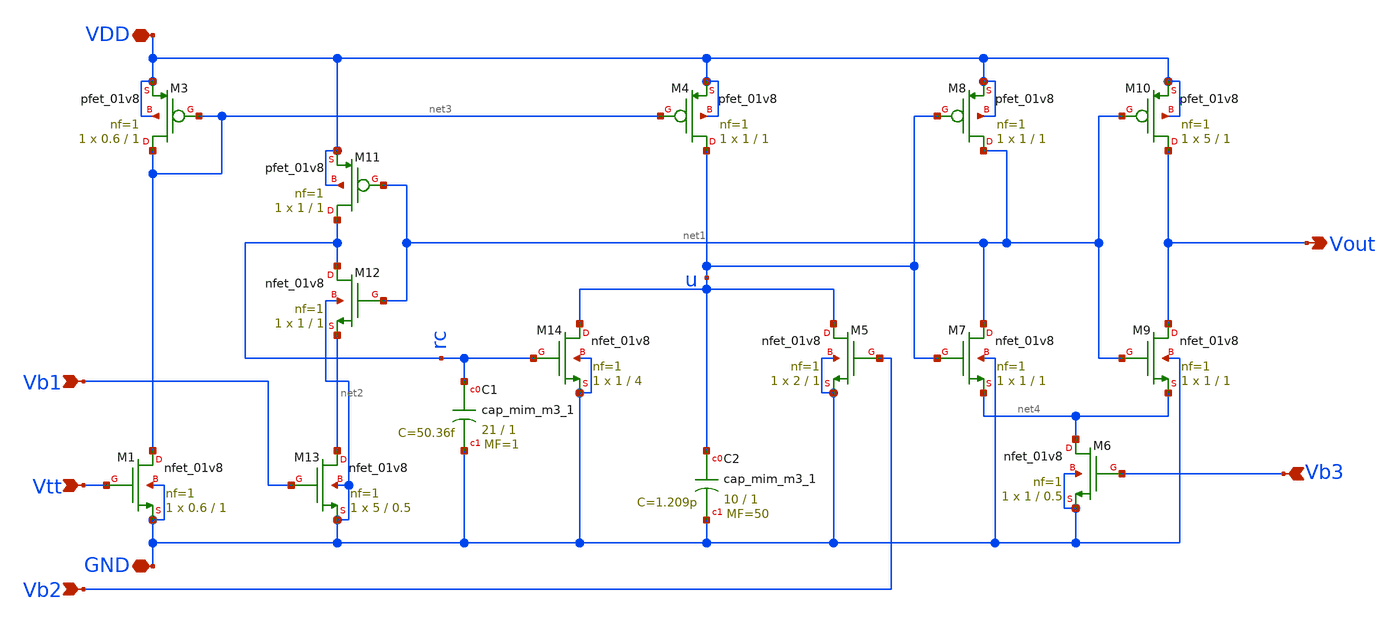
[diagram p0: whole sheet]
** sch_path: LIF_neuron/LIF_neuron_Vohra_modified.sch
**.subckt LIF_neuron_Vohra_modified Vtt GND Vb1 Vb2 VDD Vout Vb3
*.ipin Vtt
*.iopin GND
*.ipin Vb1
*.ipin Vb2
*.iopin VDD
*.opin Vout
*.ipin Vb3
XM1 net3 Vtt GND GND sky130_fd_pr__nfet_01v8 L=1 W=0.6 nf=1 ad='int((nf+1)/2) * W/nf * 0.29' as='int((nf+2)/2) * W/nf * 0.29'
+ pd='2*int((nf+1)/2) * (W/nf + 0.29)' ps='2*int((nf+2)/2) * (W/nf + 0.29)' nrd='0.29 / W' nrs='0.29 / W'
+ sa=0 sb=0 sd=0 mult=1 m=1
XM3 net3 net3 VDD VDD sky130_fd_pr__pfet_01v8 L=1 W=0.6 nf=1 ad='int((nf+1)/2) * W/nf * 0.29' as='int((nf+2)/2) * W/nf * 0.29'
+ pd='2*int((nf+1)/2) * (W/nf + 0.29)' ps='2*int((nf+2)/2) * (W/nf + 0.29)' nrd='0.29 / W' nrs='0.29 / W'
+ sa=0 sb=0 sd=0 mult=1 m=1
XM13 net2 Vb1 GND GND sky130_fd_pr__nfet_01v8 L=0.5 W=5 nf=1 ad='int((nf+1)/2) * W/nf * 0.29' as='int((nf+2)/2) * W/nf * 0.29'
+ pd='2*int((nf+1)/2) * (W/nf + 0.29)' ps='2*int((nf+2)/2) * (W/nf + 0.29)' nrd='0.29 / W' nrs='0.29 / W'
+ sa=0 sb=0 sd=0 mult=1 m=1
XM12 rc net1 net2 GND sky130_fd_pr__nfet_01v8 L=1 W=1 nf=1 ad='int((nf+1)/2) * W/nf * 0.29' as='int((nf+2)/2) * W/nf * 0.29'
+ pd='2*int((nf+1)/2) * (W/nf + 0.29)' ps='2*int((nf+2)/2) * (W/nf + 0.29)' nrd='0.29 / W' nrs='0.29 / W'
+ sa=0 sb=0 sd=0 mult=1 m=1
XM11 rc net1 VDD VDD sky130_fd_pr__pfet_01v8 L=1 W=1 nf=1 ad='int((nf+1)/2) * W/nf * 0.29' as='int((nf+2)/2) * W/nf * 0.29'
+ pd='2*int((nf+1)/2) * (W/nf + 0.29)' ps='2*int((nf+2)/2) * (W/nf + 0.29)' nrd='0.29 / W' nrs='0.29 / W'
+ sa=0 sb=0 sd=0 mult=1 m=1
XC1 rc GND sky130_fd_pr__cap_mim_m3_1 W=21 L=1 MF=1 m=1
XM14 u rc GND GND sky130_fd_pr__nfet_01v8 L=4 W=1 nf=1 ad='int((nf+1)/2) * W/nf * 0.29' as='int((nf+2)/2) * W/nf * 0.29'
+ pd='2*int((nf+1)/2) * (W/nf + 0.29)' ps='2*int((nf+2)/2) * (W/nf + 0.29)' nrd='0.29 / W' nrs='0.29 / W'
+ sa=0 sb=0 sd=0 mult=1 m=1
XM4 u net3 VDD VDD sky130_fd_pr__pfet_01v8 L=1 W=1 nf=1 ad='int((nf+1)/2) * W/nf * 0.29' as='int((nf+2)/2) * W/nf * 0.29'
+ pd='2*int((nf+1)/2) * (W/nf + 0.29)' ps='2*int((nf+2)/2) * (W/nf + 0.29)' nrd='0.29 / W' nrs='0.29 / W'
+ sa=0 sb=0 sd=0 mult=1 m=1
XC2 u GND sky130_fd_pr__cap_mim_m3_1 W=10 L=1 MF=50 m=50
XM5 u Vb2 GND GND sky130_fd_pr__nfet_01v8 L=1 W=2 nf=1 ad='int((nf+1)/2) * W/nf * 0.29' as='int((nf+2)/2) * W/nf * 0.29'
+ pd='2*int((nf+1)/2) * (W/nf + 0.29)' ps='2*int((nf+2)/2) * (W/nf + 0.29)' nrd='0.29 / W' nrs='0.29 / W'
+ sa=0 sb=0 sd=0 mult=1 m=1
XM6 net4 Vb3 GND GND sky130_fd_pr__nfet_01v8 L=0.5 W=1 nf=1 ad='int((nf+1)/2) * W/nf * 0.29' as='int((nf+2)/2) * W/nf * 0.29'
+ pd='2*int((nf+1)/2) * (W/nf + 0.29)' ps='2*int((nf+2)/2) * (W/nf + 0.29)' nrd='0.29 / W' nrs='0.29 / W'
+ sa=0 sb=0 sd=0 mult=1 m=1
XM7 net1 u net4 GND sky130_fd_pr__nfet_01v8 L=1 W=1 nf=1 ad='int((nf+1)/2) * W/nf * 0.29' as='int((nf+2)/2) * W/nf * 0.29'
+ pd='2*int((nf+1)/2) * (W/nf + 0.29)' ps='2*int((nf+2)/2) * (W/nf + 0.29)' nrd='0.29 / W' nrs='0.29 / W'
+ sa=0 sb=0 sd=0 mult=1 m=1
XM8 net1 u VDD VDD sky130_fd_pr__pfet_01v8 L=1 W=1 nf=1 ad='int((nf+1)/2) * W/nf * 0.29' as='int((nf+2)/2) * W/nf * 0.29'
+ pd='2*int((nf+1)/2) * (W/nf + 0.29)' ps='2*int((nf+2)/2) * (W/nf + 0.29)' nrd='0.29 / W' nrs='0.29 / W'
+ sa=0 sb=0 sd=0 mult=1 m=1
XM9 Vout net1 net4 GND sky130_fd_pr__nfet_01v8 L=1 W=1 nf=1 ad='int((nf+1)/2) * W/nf * 0.29' as='int((nf+2)/2) * W/nf * 0.29'
+ pd='2*int((nf+1)/2) * (W/nf + 0.29)' ps='2*int((nf+2)/2) * (W/nf + 0.29)' nrd='0.29 / W' nrs='0.29 / W'
+ sa=0 sb=0 sd=0 mult=1 m=1
XM10 Vout net1 VDD VDD sky130_fd_pr__pfet_01v8 L=1 W=5 nf=1 ad='int((nf+1)/2) * W/nf * 0.29' as='int((nf+2)/2) * W/nf * 0.29'
+ pd='2*int((nf+1)/2) * (W/nf + 0.29)' ps='2*int((nf+2)/2) * (W/nf + 0.29)' nrd='0.29 / W' nrs='0.29 / W'
+ sa=0 sb=0 sd=0 mult=1 m=1
**.ends
.end
